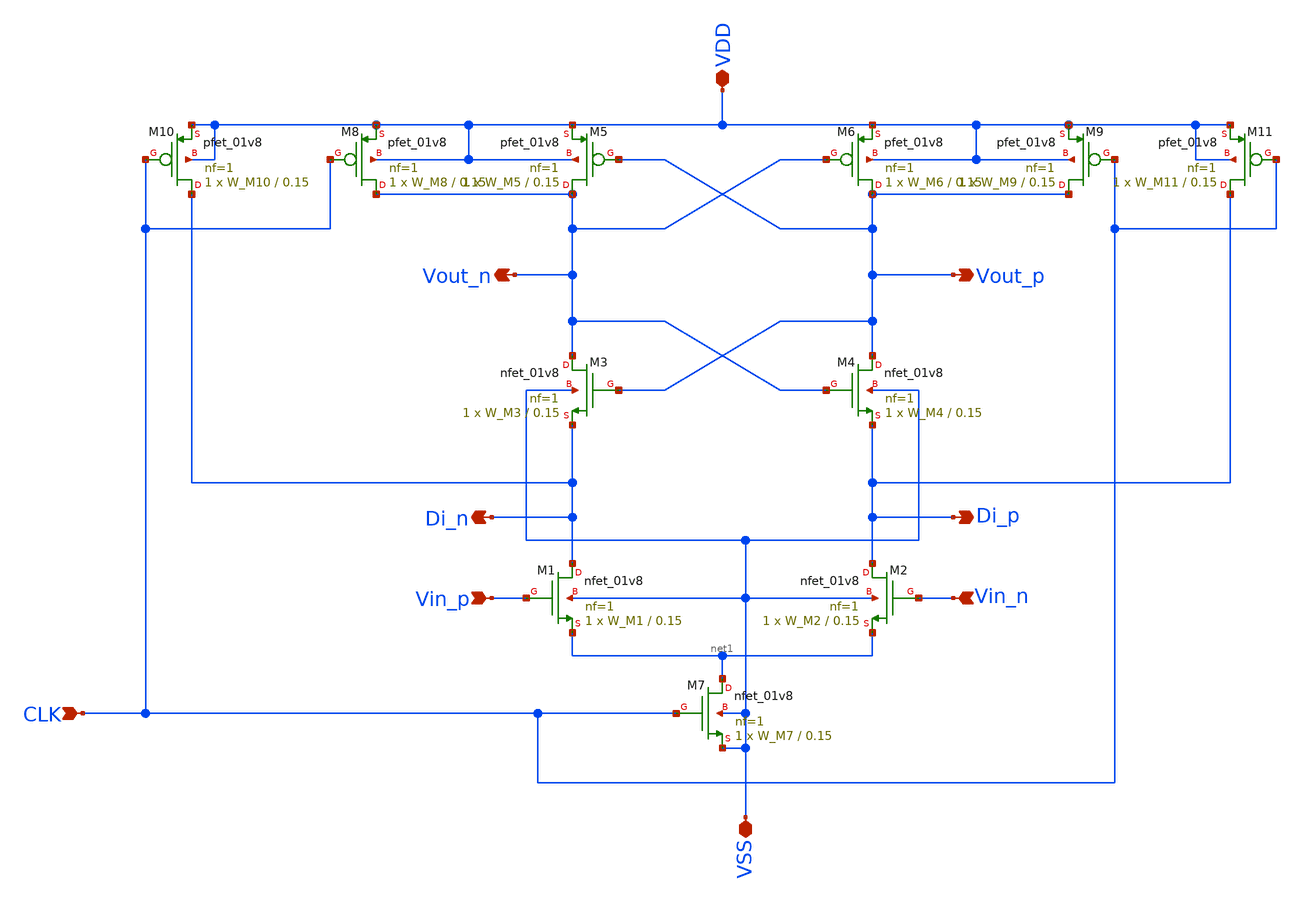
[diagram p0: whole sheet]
** sch_path: xschem/strong_arm_comp.sch
**.subckt strong_arm_comp Vin_p Vin_n CLK VDD Vout_n Vout_p VSS Di_n Di_p
*.ipin Vin_p
*.ipin Vin_n
*.ipin CLK
*.iopin VDD
*.opin Vout_n
*.opin Vout_p
*.iopin VSS
*.opin Di_n
*.opin Di_p
XM1 Di_n Vin_p net1 VSS sky130_fd_pr__nfet_01v8 L=0.15 W=W_M1 nf=1 ad='int((nf+1)/2) * W/nf * 0.29' as='int((nf+2)/2) * W/nf * 0.29'
+ pd='2*int((nf+1)/2) * (W/nf + 0.29)' ps='2*int((nf+2)/2) * (W/nf + 0.29)' nrd='0.29 / W' nrs='0.29 / W'
+ sa=0 sb=0 sd=0 mult=1 m=1
XM2 Di_p Vin_n net1 VSS sky130_fd_pr__nfet_01v8 L=0.15 W=W_M2 nf=1 ad='int((nf+1)/2) * W/nf * 0.29' as='int((nf+2)/2) * W/nf * 0.29'
+ pd='2*int((nf+1)/2) * (W/nf + 0.29)' ps='2*int((nf+2)/2) * (W/nf + 0.29)' nrd='0.29 / W' nrs='0.29 / W'
+ sa=0 sb=0 sd=0 mult=1 m=1
XM3 Vout_n Vout_p Di_n VSS sky130_fd_pr__nfet_01v8 L=0.15 W=W_M3 nf=1 ad='int((nf+1)/2) * W/nf * 0.29'
+ as='int((nf+2)/2) * W/nf * 0.29' pd='2*int((nf+1)/2) * (W/nf + 0.29)' ps='2*int((nf+2)/2) * (W/nf + 0.29)'
+ nrd='0.29 / W' nrs='0.29 / W' sa=0 sb=0 sd=0 mult=1 m=1
XM4 Vout_p Vout_n Di_p VSS sky130_fd_pr__nfet_01v8 L=0.15 W=W_M4 nf=1 ad='int((nf+1)/2) * W/nf * 0.29'
+ as='int((nf+2)/2) * W/nf * 0.29' pd='2*int((nf+1)/2) * (W/nf + 0.29)' ps='2*int((nf+2)/2) * (W/nf + 0.29)'
+ nrd='0.29 / W' nrs='0.29 / W' sa=0 sb=0 sd=0 mult=1 m=1
XM5 Vout_n Vout_p VDD VDD sky130_fd_pr__pfet_01v8 L=0.15 W=W_M5 nf=1 ad='int((nf+1)/2) * W/nf * 0.29'
+ as='int((nf+2)/2) * W/nf * 0.29' pd='2*int((nf+1)/2) * (W/nf + 0.29)' ps='2*int((nf+2)/2) * (W/nf + 0.29)'
+ nrd='0.29 / W' nrs='0.29 / W' sa=0 sb=0 sd=0 mult=1 m=1
XM6 Vout_p Vout_n VDD VDD sky130_fd_pr__pfet_01v8 L=0.15 W=W_M6 nf=1 ad='int((nf+1)/2) * W/nf * 0.29'
+ as='int((nf+2)/2) * W/nf * 0.29' pd='2*int((nf+1)/2) * (W/nf + 0.29)' ps='2*int((nf+2)/2) * (W/nf + 0.29)'
+ nrd='0.29 / W' nrs='0.29 / W' sa=0 sb=0 sd=0 mult=1 m=1
XM9 Vout_p CLK VDD VDD sky130_fd_pr__pfet_01v8 L=0.15 W=W_M9 nf=1 ad='int((nf+1)/2) * W/nf * 0.29' as='int((nf+2)/2) * W/nf * 0.29'
+ pd='2*int((nf+1)/2) * (W/nf + 0.29)' ps='2*int((nf+2)/2) * (W/nf + 0.29)' nrd='0.29 / W' nrs='0.29 / W'
+ sa=0 sb=0 sd=0 mult=1 m=1
XM8 Vout_n CLK VDD VDD sky130_fd_pr__pfet_01v8 L=0.15 W=W_M8 nf=1 ad='int((nf+1)/2) * W/nf * 0.29' as='int((nf+2)/2) * W/nf * 0.29'
+ pd='2*int((nf+1)/2) * (W/nf + 0.29)' ps='2*int((nf+2)/2) * (W/nf + 0.29)' nrd='0.29 / W' nrs='0.29 / W'
+ sa=0 sb=0 sd=0 mult=1 m=1
XM7 net1 CLK VSS VSS sky130_fd_pr__nfet_01v8 L=0.15 W=W_M7 nf=1 ad='int((nf+1)/2) * W/nf * 0.29' as='int((nf+2)/2) * W/nf * 0.29'
+ pd='2*int((nf+1)/2) * (W/nf + 0.29)' ps='2*int((nf+2)/2) * (W/nf + 0.29)' nrd='0.29 / W' nrs='0.29 / W'
+ sa=0 sb=0 sd=0 mult=1 m=1
XM10 Di_n CLK VDD VDD sky130_fd_pr__pfet_01v8 L=0.15 W=W_M10 nf=1 ad='int((nf+1)/2) * W/nf * 0.29' as='int((nf+2)/2) * W/nf * 0.29'
+ pd='2*int((nf+1)/2) * (W/nf + 0.29)' ps='2*int((nf+2)/2) * (W/nf + 0.29)' nrd='0.29 / W' nrs='0.29 / W'
+ sa=0 sb=0 sd=0 mult=1 m=1
XM11 Di_p CLK VDD VDD sky130_fd_pr__pfet_01v8 L=0.15 W=W_M11 nf=1 ad='int((nf+1)/2) * W/nf * 0.29' as='int((nf+2)/2) * W/nf * 0.29'
+ pd='2*int((nf+1)/2) * (W/nf + 0.29)' ps='2*int((nf+2)/2) * (W/nf + 0.29)' nrd='0.29 / W' nrs='0.29 / W'
+ sa=0 sb=0 sd=0 mult=1 m=1
**.ends
.end
